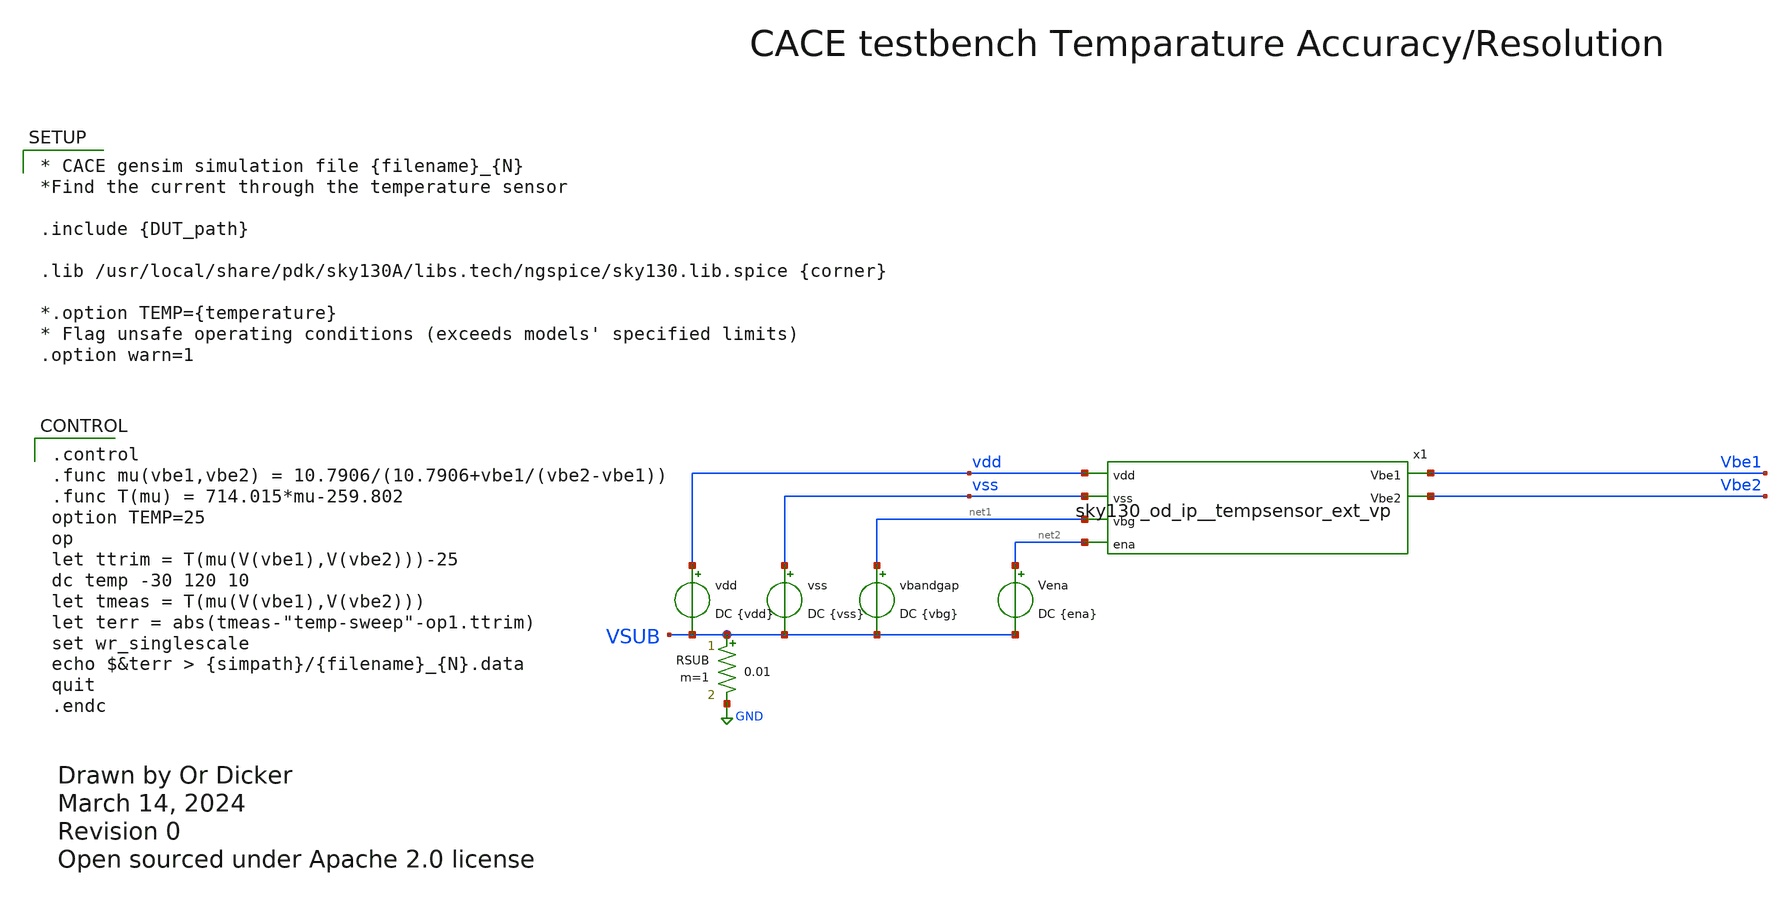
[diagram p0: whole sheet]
** sch_path: cace/templates/temperature_all.sch
* Open sourced under Apache 2.0 license
**.subckt temperature_all
vss vss VSUB DC {vss}
vdd vdd VSUB DC {vdd}
RSUB VSUB GND 0.01 m=1
Vena net2 VSUB DC {ena}
x1 vdd vss net1 Vbe1 Vbe2 net2 sky130_od_ip__tempsensor_ext_vp
vbandgap net1 VSUB DC {vbg}
**** begin user architecture code

.control
.func mu(vbe1,vbe2) = 10.7906/(10.7906+vbe1/(vbe2-vbe1))
.func T(mu) = 714.015*mu-259.802
option TEMP=25
op
let ttrim = T(mu(V(vbe1),V(vbe2)))-25
dc temp -30 120 10
let tmeas = T(mu(V(vbe1),V(vbe2)))
let terr = abs(tmeas-"temp-sweep"-op1.ttrim)
set wr_singlescale
echo $&terr > {simpath}/{filename}_{N}.data
quit
.endc



* CACE gensim simulation file {filename}_{N}
*Find the current through the temperature sensor

.include {DUT_path}

.lib /usr/local/share/pdk/sky130A/libs.tech/ngspice/sky130.lib.spice {corner}

*.option TEMP={temperature}
* Flag unsafe operating conditions (exceeds models' specified limits)
.option warn=1


**** end user architecture code
**.ends
.GLOBAL GND
.end
